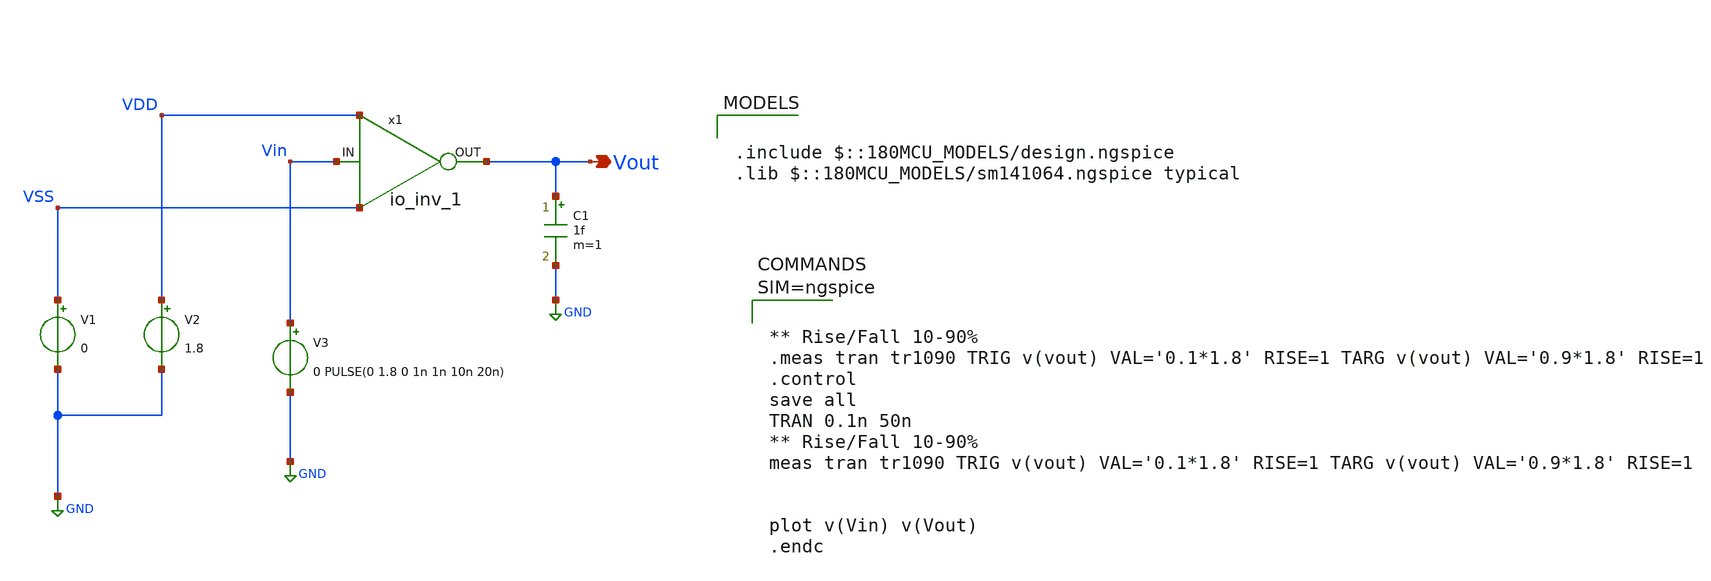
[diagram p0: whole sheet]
** sch_path: xschem/io_inv_1_tb.sch
* Copyright 2023 David Mitchell Bailey
* Licensed under the Apache License, Version 2.0 (the "License");
* you may not use this file except in compliance with the License.
* You may obtain a copy of the License at
* https://www.apache.org/licenses/LICENSE-2.0
* Unless required by applicable law or agreed to in writing, software
* distributed under the License is distributed on an "AS IS" BASIS,
* WITHOUT WARRANTIES OR CONDITIONS OF ANY KIND, either express or implied.
* See the License for the specific language governing permissions and
* limitations under the License.
**.subckt io_inv_1_tb Vout
*.opin Vout
x1 Vin Vout VDD VSS io_inv_1
V1 VSS GND 0
V2 VDD GND 1.8
V3 Vin GND 0 PULSE(0 1.8 0 1n 1n 10n 20n)
C1 Vout GND 1f m=1
**** begin user architecture code

.include $::180MCU_MODELS/design.ngspice
.lib $::180MCU_MODELS/sm141064.ngspice typical




** Rise/Fall 10-90%
.meas tran tr1090 TRIG v(vout) VAL='0.1*1.8' RISE=1 TARG v(vout) VAL='0.9*1.8' RISE=1
.control
save all
TRAN 0.1n 50n
** Rise/Fall 10-90%
meas tran tr1090 TRIG v(vout) VAL='0.1*1.8' RISE=1 TARG v(vout) VAL='0.9*1.8' RISE=1


plot v(Vin) v(Vout)
.endc




**** end user architecture code
**.ends
.GLOBAL GND
.end
